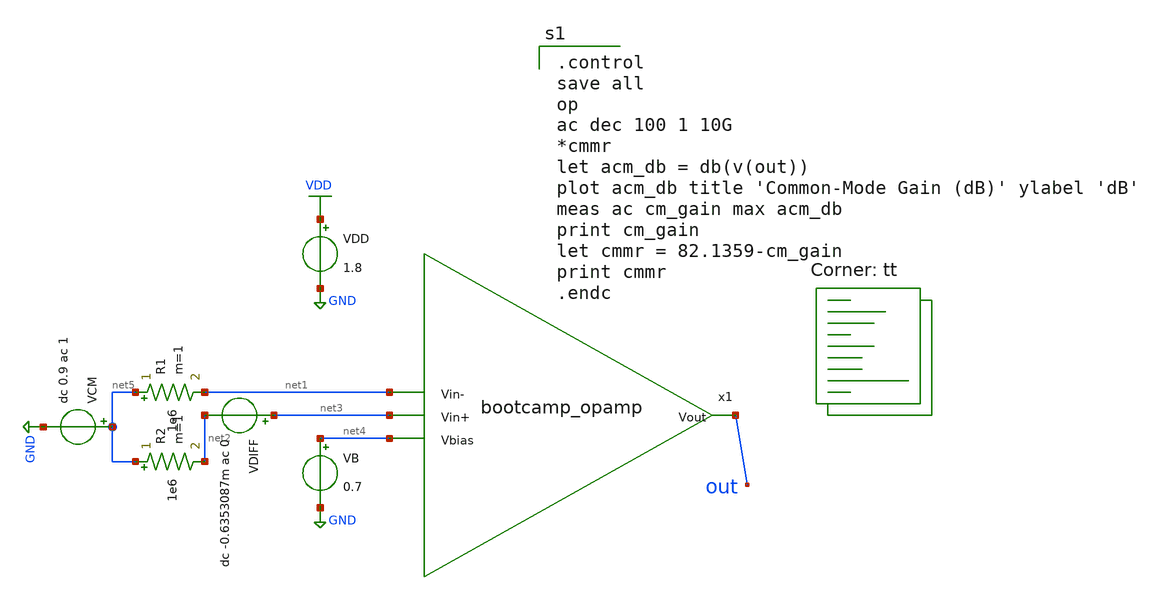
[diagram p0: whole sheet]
** sch_path: analog/schematics/tb_cmrr.sch
**.subckt tb_cmrr
x1 out net1 net3 net4 bootcamp_opamp
VDD VDD GND 1.8
VCM net5 GND dc 0.9 ac 1
VB net4 GND 0.7
R1 net5 net1 1e6 m=1
R2 net5 net2 1e6 m=1
VDIFF net3 net2 dc -0.6353087m ac 0
**** begin user architecture code
.lib $::SKYWATER_MODELS/sky130.lib.spice tt

.control
save all
op
ac dec 100 1 10G
*cmmr
let acm_db = db(v(out))
plot acm_db title 'Common-Mode Gain (dB)' ylabel 'dB'
meas ac cm_gain max acm_db
print cm_gain
let cmmr = 82.1359-cm_gain
print cmmr
.endc

**** end user architecture code
**.ends
.GLOBAL GND
.GLOBAL VDD
.end
